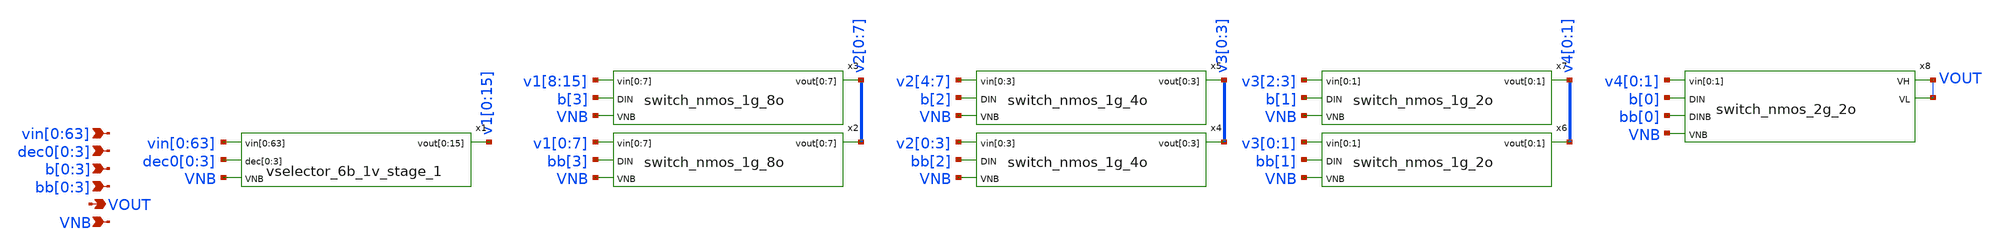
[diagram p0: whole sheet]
** sch_path: xschem/vselector_seg1.sch
**.subckt vselector_seg1
*+ vin[0],vin[1],vin[2],vin[3],vin[4],vin[5],vin[6],vin[7],vin[8],vin[9],vin[10],vin[11],vin[12],vin[13],vin[14],vin[15],vin[16],vin[17],vin[18],vin[19],vin[20],vin[21],vin[22],vin[23],vin[24],vin[25],vin[26],vin[27],vin[28],vin[29],vin[30],vin[31],vin[32],vin[33],vin[34],vin[35],vin[36],vin[37],vin[38],vin[39],vin[40],vin[41],vin[42],vin[43],vin[44],vin[45],vin[46],vin[47],vin[48],vin[49],vin[50],vin[51],vin[52],vin[53],vin[54],vin[55],vin[56],vin[57],vin[58],vin[59],vin[60],vin[61],vin[62],vin[63] VOUT VNB dec0[0],dec0[1],dec0[2],dec0[3] b[0],b[1],b[2],b[3] bb[0],bb[1],bb[2],bb[3]
*.ipin
*+ vin[0],vin[1],vin[2],vin[3],vin[4],vin[5],vin[6],vin[7],vin[8],vin[9],vin[10],vin[11],vin[12],vin[13],vin[14],vin[15],vin[16],vin[17],vin[18],vin[19],vin[20],vin[21],vin[22],vin[23],vin[24],vin[25],vin[26],vin[27],vin[28],vin[29],vin[30],vin[31],vin[32],vin[33],vin[34],vin[35],vin[36],vin[37],vin[38],vin[39],vin[40],vin[41],vin[42],vin[43],vin[44],vin[45],vin[46],vin[47],vin[48],vin[49],vin[50],vin[51],vin[52],vin[53],vin[54],vin[55],vin[56],vin[57],vin[58],vin[59],vin[60],vin[61],vin[62],vin[63]
*.opin VOUT
*.ipin VNB
*.ipin dec0[0],dec0[1],dec0[2],dec0[3]
*.ipin b[0],b[1],b[2],b[3]
*.ipin bb[0],bb[1],bb[2],bb[3]
x1 vin[0] vin[1] vin[2] vin[3] vin[4] vin[5] vin[6] vin[7] vin[8] vin[9] vin[10] vin[11] vin[12]
+ vin[13] vin[14] vin[15] vin[16] vin[17] vin[18] vin[19] vin[20] vin[21] vin[22] vin[23] vin[24] vin[25]
+ vin[26] vin[27] vin[28] vin[29] vin[30] vin[31] vin[32] vin[33] vin[34] vin[35] vin[36] vin[37] vin[38]
+ vin[39] vin[40] vin[41] vin[42] vin[43] vin[44] vin[45] vin[46] vin[47] vin[48] vin[49] vin[50] vin[51]
+ vin[52] vin[53] vin[54] vin[55] vin[56] vin[57] vin[58] vin[59] vin[60] vin[61] vin[62] vin[63] dec0[0]
+ dec0[1] dec0[2] dec0[3] v1[0] v1[1] v1[2] v1[3] v1[4] v1[5] v1[6] v1[7] v1[8] v1[9] v1[10] v1[11] v1[12]
+ v1[13] v1[14] v1[15] VNB vselector_6b_1v_stage_1
x2 v1[0] v1[1] v1[2] v1[3] v1[4] v1[5] v1[6] v1[7] bb[3] v2[0] v2[1] v2[2] v2[3] v2[4] v2[5] v2[6]
+ v2[7] VNB switch_nmos_1g_8o
x3 v1[8] v1[9] v1[10] v1[11] v1[12] v1[13] v1[14] v1[15] b[3] v2[0] v2[1] v2[2] v2[3] v2[4] v2[5]
+ v2[6] v2[7] VNB switch_nmos_1g_8o
x4 v2[0] v2[1] v2[2] v2[3] bb[2] v3[0] v3[1] v3[2] v3[3] VNB switch_nmos_1g_4o
x5 v2[4] v2[5] v2[6] v2[7] b[2] v3[0] v3[1] v3[2] v3[3] VNB switch_nmos_1g_4o
x6 v3[0] v3[1] bb[1] v4[0] v4[1] VNB switch_nmos_1g_2o
x7 v3[2] v3[3] b[1] v4[0] v4[1] VNB switch_nmos_1g_2o
x8 v4[0] v4[1] b[0] bb[0] VOUT VOUT VNB switch_nmos_2g_2o
**.ends

* expanding   symbol:  vselector_6b_1v_stage_1.sym # of pins=4
** sym_path: xschem/vselector_6b_1v_stage_1.sym
** sch_path: xschem/vselector_6b_1v_stage_1.sch
.subckt vselector_6b_1v_stage_1 vin[0] vin[1] vin[2] vin[3] vin[4] vin[5] vin[6] vin[7] vin[8]
+ vin[9] vin[10] vin[11] vin[12] vin[13] vin[14] vin[15] vin[16] vin[17] vin[18] vin[19] vin[20] vin[21]
+ vin[22] vin[23] vin[24] vin[25] vin[26] vin[27] vin[28] vin[29] vin[30] vin[31] vin[32] vin[33] vin[34]
+ vin[35] vin[36] vin[37] vin[38] vin[39] vin[40] vin[41] vin[42] vin[43] vin[44] vin[45] vin[46] vin[47]
+ vin[48] vin[49] vin[50] vin[51] vin[52] vin[53] vin[54] vin[55] vin[56] vin[57] vin[58] vin[59] vin[60]
+ vin[61] vin[62] vin[63] dec[0] dec[1] dec[2] dec[3] vout[0] vout[1] vout[2] vout[3] vout[4] vout[5] vout[6]
+ vout[7] vout[8] vout[9] vout[10] vout[11] vout[12] vout[13] vout[14] vout[15] VNB
*.ipin
*+ vin[0],vin[1],vin[2],vin[3],vin[4],vin[5],vin[6],vin[7],vin[8],vin[9],vin[10],vin[11],vin[12],vin[13],vin[14],vin[15],vin[16],vin[17],vin[18],vin[19],vin[20],vin[21],vin[22],vin[23],vin[24],vin[25],vin[26],vin[27],vin[28],vin[29],vin[30],vin[31],vin[32],vin[33],vin[34],vin[35],vin[36],vin[37],vin[38],vin[39],vin[40],vin[41],vin[42],vin[43],vin[44],vin[45],vin[46],vin[47],vin[48],vin[49],vin[50],vin[51],vin[52],vin[53],vin[54],vin[55],vin[56],vin[57],vin[58],vin[59],vin[60],vin[61],vin[62],vin[63]
*.opin
*+ vout[0],vout[1],vout[2],vout[3],vout[4],vout[5],vout[6],vout[7],vout[8],vout[9],vout[10],vout[11],vout[12],vout[13],vout[14],vout[15]
*.ipin VNB
*.ipin dec[0],dec[1],dec[2],dec[3]
x1 vin[48] vin[49] vin[50] vin[51] vin[52] vin[53] vin[54] vin[55] vin[56] vin[57] vin[58] vin[59]
+ vin[60] vin[61] vin[62] vin[63] dec[3] vout[0] vout[1] vout[2] vout[3] vout[4] vout[5] vout[6] vout[7]
+ vout[8] vout[9] vout[10] vout[11] vout[12] vout[13] vout[14] vout[15] VNB vselector_16b_1v
x2 vin[32] vin[33] vin[34] vin[35] vin[36] vin[37] vin[38] vin[39] vin[40] vin[41] vin[42] vin[43]
+ vin[44] vin[45] vin[46] vin[47] dec[2] vout[0] vout[1] vout[2] vout[3] vout[4] vout[5] vout[6] vout[7]
+ vout[8] vout[9] vout[10] vout[11] vout[12] vout[13] vout[14] vout[15] VNB vselector_16b_1v
x3 vin[16] vin[17] vin[18] vin[19] vin[20] vin[21] vin[22] vin[23] vin[24] vin[25] vin[26] vin[27]
+ vin[28] vin[29] vin[30] vin[31] dec[1] vout[0] vout[1] vout[2] vout[3] vout[4] vout[5] vout[6] vout[7]
+ vout[8] vout[9] vout[10] vout[11] vout[12] vout[13] vout[14] vout[15] VNB vselector_16b_1v
x4 vin[0] vin[1] vin[2] vin[3] vin[4] vin[5] vin[6] vin[7] vin[8] vin[9] vin[10] vin[11] vin[12]
+ vin[13] vin[14] vin[15] dec[0] vout[0] vout[1] vout[2] vout[3] vout[4] vout[5] vout[6] vout[7] vout[8]
+ vout[9] vout[10] vout[11] vout[12] vout[13] vout[14] vout[15] VNB vselector_16b_1v
.ends


* expanding   symbol:  switch_nmos_1g_8o.sym # of pins=4
** sym_path: xschem/switch_nmos_1g_8o.sym
** sch_path: xschem/switch_nmos_1g_8o.sch
.subckt switch_nmos_1g_8o vin[0] vin[1] vin[2] vin[3] vin[4] vin[5] vin[6] vin[7] DIN vout[0]
+ vout[1] vout[2] vout[3] vout[4] vout[5] vout[6] vout[7] VNB
*.ipin vin[0],vin[1],vin[2],vin[3],vin[4],vin[5],vin[6],vin[7]
*.opin vout[0],vout[1],vout[2],vout[3],vout[4],vout[5],vout[6],vout[7]
*.ipin VNB
*.ipin DIN
.param wp=0.42 wn=0.42 l=0.5

XM1 vin[0] DIN vout[0] VNB sky130_fd_pr__nfet_g5v0d10v5 L=l W=wn nf=1 ad='int((nf+1)/2) * W/nf * 0.29'
+ as='int((nf+2)/2) * W/nf * 0.29' pd='2*int((nf+1)/2) * (W/nf + 0.29)' ps='2*int((nf+2)/2) * (W/nf + 0.29)'
+ nrd='0.29 / W' nrs='0.29 / W' sa=0 sb=0 sd=0 mult=1 m=1
XM2 vin[1] DIN vout[1] VNB sky130_fd_pr__nfet_g5v0d10v5 L=l W=wn nf=1 ad='int((nf+1)/2) * W/nf * 0.29'
+ as='int((nf+2)/2) * W/nf * 0.29' pd='2*int((nf+1)/2) * (W/nf + 0.29)' ps='2*int((nf+2)/2) * (W/nf + 0.29)'
+ nrd='0.29 / W' nrs='0.29 / W' sa=0 sb=0 sd=0 mult=1 m=1
XM3 vin[2] DIN vout[2] VNB sky130_fd_pr__nfet_g5v0d10v5 L=l W=wn nf=1 ad='int((nf+1)/2) * W/nf * 0.29'
+ as='int((nf+2)/2) * W/nf * 0.29' pd='2*int((nf+1)/2) * (W/nf + 0.29)' ps='2*int((nf+2)/2) * (W/nf + 0.29)'
+ nrd='0.29 / W' nrs='0.29 / W' sa=0 sb=0 sd=0 mult=1 m=1
XM4 vin[3] DIN vout[3] VNB sky130_fd_pr__nfet_g5v0d10v5 L=l W=wn nf=1 ad='int((nf+1)/2) * W/nf * 0.29'
+ as='int((nf+2)/2) * W/nf * 0.29' pd='2*int((nf+1)/2) * (W/nf + 0.29)' ps='2*int((nf+2)/2) * (W/nf + 0.29)'
+ nrd='0.29 / W' nrs='0.29 / W' sa=0 sb=0 sd=0 mult=1 m=1
XM5 vin[4] DIN vout[4] VNB sky130_fd_pr__nfet_g5v0d10v5 L=l W=wn nf=1 ad='int((nf+1)/2) * W/nf * 0.29'
+ as='int((nf+2)/2) * W/nf * 0.29' pd='2*int((nf+1)/2) * (W/nf + 0.29)' ps='2*int((nf+2)/2) * (W/nf + 0.29)'
+ nrd='0.29 / W' nrs='0.29 / W' sa=0 sb=0 sd=0 mult=1 m=1
XM6 vin[5] DIN vout[5] VNB sky130_fd_pr__nfet_g5v0d10v5 L=l W=wn nf=1 ad='int((nf+1)/2) * W/nf * 0.29'
+ as='int((nf+2)/2) * W/nf * 0.29' pd='2*int((nf+1)/2) * (W/nf + 0.29)' ps='2*int((nf+2)/2) * (W/nf + 0.29)'
+ nrd='0.29 / W' nrs='0.29 / W' sa=0 sb=0 sd=0 mult=1 m=1
XM7 vin[6] DIN vout[6] VNB sky130_fd_pr__nfet_g5v0d10v5 L=l W=wn nf=1 ad='int((nf+1)/2) * W/nf * 0.29'
+ as='int((nf+2)/2) * W/nf * 0.29' pd='2*int((nf+1)/2) * (W/nf + 0.29)' ps='2*int((nf+2)/2) * (W/nf + 0.29)'
+ nrd='0.29 / W' nrs='0.29 / W' sa=0 sb=0 sd=0 mult=1 m=1
XM8 vin[7] DIN vout[7] VNB sky130_fd_pr__nfet_g5v0d10v5 L=l W=wn nf=1 ad='int((nf+1)/2) * W/nf * 0.29'
+ as='int((nf+2)/2) * W/nf * 0.29' pd='2*int((nf+1)/2) * (W/nf + 0.29)' ps='2*int((nf+2)/2) * (W/nf + 0.29)'
+ nrd='0.29 / W' nrs='0.29 / W' sa=0 sb=0 sd=0 mult=1 m=1
.ends


* expanding   symbol:  switch_nmos_1g_4o.sym # of pins=4
** sym_path: xschem/switch_nmos_1g_4o.sym
** sch_path: xschem/switch_nmos_1g_4o.sch
.subckt switch_nmos_1g_4o vin[0] vin[1] vin[2] vin[3] DIN vout[0] vout[1] vout[2] vout[3] VNB
*.ipin vin[0],vin[1],vin[2],vin[3]
*.opin vout[0],vout[1],vout[2],vout[3]
*.ipin VNB
*.ipin DIN
.param wp=0.42 wn=0.42 l=0.5

XM1 vin[0] DIN vout[0] VNB sky130_fd_pr__nfet_g5v0d10v5 L=l W=wn nf=1 ad='int((nf+1)/2) * W/nf * 0.29'
+ as='int((nf+2)/2) * W/nf * 0.29' pd='2*int((nf+1)/2) * (W/nf + 0.29)' ps='2*int((nf+2)/2) * (W/nf + 0.29)'
+ nrd='0.29 / W' nrs='0.29 / W' sa=0 sb=0 sd=0 mult=1 m=1
XM2 vin[1] DIN vout[1] VNB sky130_fd_pr__nfet_g5v0d10v5 L=l W=wn nf=1 ad='int((nf+1)/2) * W/nf * 0.29'
+ as='int((nf+2)/2) * W/nf * 0.29' pd='2*int((nf+1)/2) * (W/nf + 0.29)' ps='2*int((nf+2)/2) * (W/nf + 0.29)'
+ nrd='0.29 / W' nrs='0.29 / W' sa=0 sb=0 sd=0 mult=1 m=1
XM3 vin[2] DIN vout[2] VNB sky130_fd_pr__nfet_g5v0d10v5 L=l W=wn nf=1 ad='int((nf+1)/2) * W/nf * 0.29'
+ as='int((nf+2)/2) * W/nf * 0.29' pd='2*int((nf+1)/2) * (W/nf + 0.29)' ps='2*int((nf+2)/2) * (W/nf + 0.29)'
+ nrd='0.29 / W' nrs='0.29 / W' sa=0 sb=0 sd=0 mult=1 m=1
XM4 vin[3] DIN vout[3] VNB sky130_fd_pr__nfet_g5v0d10v5 L=l W=wn nf=1 ad='int((nf+1)/2) * W/nf * 0.29'
+ as='int((nf+2)/2) * W/nf * 0.29' pd='2*int((nf+1)/2) * (W/nf + 0.29)' ps='2*int((nf+2)/2) * (W/nf + 0.29)'
+ nrd='0.29 / W' nrs='0.29 / W' sa=0 sb=0 sd=0 mult=1 m=1
.ends


* expanding   symbol:  switch_nmos_1g_2o.sym # of pins=4
** sym_path: xschem/switch_nmos_1g_2o.sym
** sch_path: xschem/switch_nmos_1g_2o.sch
.subckt switch_nmos_1g_2o vin[0] vin[1] DIN vout[0] vout[1] VNB
*.ipin vin[0],vin[1]
*.opin vout[0],vout[1]
*.ipin VNB
*.ipin DIN
.param wp=0.42 wn=0.42 l=0.5

XM2 vin[1] DIN vout[1] VNB sky130_fd_pr__nfet_g5v0d10v5 L=l W=wn nf=1 ad='int((nf+1)/2) * W/nf * 0.29'
+ as='int((nf+2)/2) * W/nf * 0.29' pd='2*int((nf+1)/2) * (W/nf + 0.29)' ps='2*int((nf+2)/2) * (W/nf + 0.29)'
+ nrd='0.29 / W' nrs='0.29 / W' sa=0 sb=0 sd=0 mult=1 m=1
XM1 vin[0] DIN vout[0] VNB sky130_fd_pr__nfet_g5v0d10v5 L=l W=wn nf=1 ad='int((nf+1)/2) * W/nf * 0.29'
+ as='int((nf+2)/2) * W/nf * 0.29' pd='2*int((nf+1)/2) * (W/nf + 0.29)' ps='2*int((nf+2)/2) * (W/nf + 0.29)'
+ nrd='0.29 / W' nrs='0.29 / W' sa=0 sb=0 sd=0 mult=1 m=1
.ends


* expanding   symbol:  switch_nmos_2g_2o.sym # of pins=6
** sym_path: xschem/switch_nmos_2g_2o.sym
** sch_path: xschem/switch_nmos_2g_2o.sch
.subckt switch_nmos_2g_2o vin[0] vin[1] DIN DINB VH VL VNB
*.ipin vin[0],vin[1]
*.opin VH
*.ipin VNB
*.ipin DIN
*.opin VL
*.ipin DINB
.param wp=0.42 wn=0.42 l=0.5

XM1 vin[0] DINB VL VNB sky130_fd_pr__nfet_g5v0d10v5 L=l W=wn nf=1 ad='int((nf+1)/2) * W/nf * 0.29' as='int((nf+2)/2) * W/nf * 0.29'
+ pd='2*int((nf+1)/2) * (W/nf + 0.29)' ps='2*int((nf+2)/2) * (W/nf + 0.29)' nrd='0.29 / W' nrs='0.29 / W'
+ sa=0 sb=0 sd=0 mult=1 m=1
XM2 vin[1] DIN VH VNB sky130_fd_pr__nfet_g5v0d10v5 L=l W=wn nf=1 ad='int((nf+1)/2) * W/nf * 0.29' as='int((nf+2)/2) * W/nf * 0.29'
+ pd='2*int((nf+1)/2) * (W/nf + 0.29)' ps='2*int((nf+2)/2) * (W/nf + 0.29)' nrd='0.29 / W' nrs='0.29 / W'
+ sa=0 sb=0 sd=0 mult=1 m=1
.ends


* expanding   symbol:  vselector_16b_1v.sym # of pins=4
** sym_path: xschem/vselector_16b_1v.sym
** sch_path: xschem/vselector_16b_1v.sch
.subckt vselector_16b_1v vin[0] vin[1] vin[2] vin[3] vin[4] vin[5] vin[6] vin[7] vin[8] vin[9]
+ vin[10] vin[11] vin[12] vin[13] vin[14] vin[15] DIN vout[0] vout[1] vout[2] vout[3] vout[4] vout[5] vout[6]
+ vout[7] vout[8] vout[9] vout[10] vout[11] vout[12] vout[13] vout[14] vout[15] VNB
*.ipin
*+ vin[0],vin[1],vin[2],vin[3],vin[4],vin[5],vin[6],vin[7],vin[8],vin[9],vin[10],vin[11],vin[12],vin[13],vin[14],vin[15]
*.opin
*+ vout[0],vout[1],vout[2],vout[3],vout[4],vout[5],vout[6],vout[7],vout[8],vout[9],vout[10],vout[11],vout[12],vout[13],vout[14],vout[15]
*.ipin VNB
*.ipin DIN
.param wp=0.42 wn=0.42 l=0.5

XM1 vout[0] DIN vin[0] VNB sky130_fd_pr__nfet_g5v0d10v5 L=l W=wn nf=1 ad='int((nf+1)/2) * W/nf * 0.29'
+ as='int((nf+2)/2) * W/nf * 0.29' pd='2*int((nf+1)/2) * (W/nf + 0.29)' ps='2*int((nf+2)/2) * (W/nf + 0.29)'
+ nrd='0.29 / W' nrs='0.29 / W' sa=0 sb=0 sd=0 mult=1 m=1
XM2 vout[1] DIN vin[1] VNB sky130_fd_pr__nfet_g5v0d10v5 L=l W=wn nf=1 ad='int((nf+1)/2) * W/nf * 0.29'
+ as='int((nf+2)/2) * W/nf * 0.29' pd='2*int((nf+1)/2) * (W/nf + 0.29)' ps='2*int((nf+2)/2) * (W/nf + 0.29)'
+ nrd='0.29 / W' nrs='0.29 / W' sa=0 sb=0 sd=0 mult=1 m=1
XM3 vout[2] DIN vin[2] VNB sky130_fd_pr__nfet_g5v0d10v5 L=l W=wn nf=1 ad='int((nf+1)/2) * W/nf * 0.29'
+ as='int((nf+2)/2) * W/nf * 0.29' pd='2*int((nf+1)/2) * (W/nf + 0.29)' ps='2*int((nf+2)/2) * (W/nf + 0.29)'
+ nrd='0.29 / W' nrs='0.29 / W' sa=0 sb=0 sd=0 mult=1 m=1
XM4 vout[3] DIN vin[3] VNB sky130_fd_pr__nfet_g5v0d10v5 L=l W=wn nf=1 ad='int((nf+1)/2) * W/nf * 0.29'
+ as='int((nf+2)/2) * W/nf * 0.29' pd='2*int((nf+1)/2) * (W/nf + 0.29)' ps='2*int((nf+2)/2) * (W/nf + 0.29)'
+ nrd='0.29 / W' nrs='0.29 / W' sa=0 sb=0 sd=0 mult=1 m=1
XM5 vout[4] DIN vin[4] VNB sky130_fd_pr__nfet_g5v0d10v5 L=l W=wn nf=1 ad='int((nf+1)/2) * W/nf * 0.29'
+ as='int((nf+2)/2) * W/nf * 0.29' pd='2*int((nf+1)/2) * (W/nf + 0.29)' ps='2*int((nf+2)/2) * (W/nf + 0.29)'
+ nrd='0.29 / W' nrs='0.29 / W' sa=0 sb=0 sd=0 mult=1 m=1
XM6 vout[5] DIN vin[5] VNB sky130_fd_pr__nfet_g5v0d10v5 L=l W=wn nf=1 ad='int((nf+1)/2) * W/nf * 0.29'
+ as='int((nf+2)/2) * W/nf * 0.29' pd='2*int((nf+1)/2) * (W/nf + 0.29)' ps='2*int((nf+2)/2) * (W/nf + 0.29)'
+ nrd='0.29 / W' nrs='0.29 / W' sa=0 sb=0 sd=0 mult=1 m=1
XM7 vout[6] DIN vin[6] VNB sky130_fd_pr__nfet_g5v0d10v5 L=l W=wn nf=1 ad='int((nf+1)/2) * W/nf * 0.29'
+ as='int((nf+2)/2) * W/nf * 0.29' pd='2*int((nf+1)/2) * (W/nf + 0.29)' ps='2*int((nf+2)/2) * (W/nf + 0.29)'
+ nrd='0.29 / W' nrs='0.29 / W' sa=0 sb=0 sd=0 mult=1 m=1
XM8 vout[7] DIN vin[7] VNB sky130_fd_pr__nfet_g5v0d10v5 L=l W=wn nf=1 ad='int((nf+1)/2) * W/nf * 0.29'
+ as='int((nf+2)/2) * W/nf * 0.29' pd='2*int((nf+1)/2) * (W/nf + 0.29)' ps='2*int((nf+2)/2) * (W/nf + 0.29)'
+ nrd='0.29 / W' nrs='0.29 / W' sa=0 sb=0 sd=0 mult=1 m=1
XM9 vout[8] DIN vin[8] VNB sky130_fd_pr__nfet_g5v0d10v5 L=l W=wn nf=1 ad='int((nf+1)/2) * W/nf * 0.29'
+ as='int((nf+2)/2) * W/nf * 0.29' pd='2*int((nf+1)/2) * (W/nf + 0.29)' ps='2*int((nf+2)/2) * (W/nf + 0.29)'
+ nrd='0.29 / W' nrs='0.29 / W' sa=0 sb=0 sd=0 mult=1 m=1
XM10 vout[9] DIN vin[9] VNB sky130_fd_pr__nfet_g5v0d10v5 L=l W=wn nf=1 ad='int((nf+1)/2) * W/nf * 0.29'
+ as='int((nf+2)/2) * W/nf * 0.29' pd='2*int((nf+1)/2) * (W/nf + 0.29)' ps='2*int((nf+2)/2) * (W/nf + 0.29)'
+ nrd='0.29 / W' nrs='0.29 / W' sa=0 sb=0 sd=0 mult=1 m=1
XM11 vout[10] DIN vin[10] VNB sky130_fd_pr__nfet_g5v0d10v5 L=l W=wn nf=1 ad='int((nf+1)/2) * W/nf * 0.29'
+ as='int((nf+2)/2) * W/nf * 0.29' pd='2*int((nf+1)/2) * (W/nf + 0.29)' ps='2*int((nf+2)/2) * (W/nf + 0.29)'
+ nrd='0.29 / W' nrs='0.29 / W' sa=0 sb=0 sd=0 mult=1 m=1
XM12 vout[11] DIN vin[11] VNB sky130_fd_pr__nfet_g5v0d10v5 L=l W=wn nf=1 ad='int((nf+1)/2) * W/nf * 0.29'
+ as='int((nf+2)/2) * W/nf * 0.29' pd='2*int((nf+1)/2) * (W/nf + 0.29)' ps='2*int((nf+2)/2) * (W/nf + 0.29)'
+ nrd='0.29 / W' nrs='0.29 / W' sa=0 sb=0 sd=0 mult=1 m=1
XM13 vout[12] DIN vin[12] VNB sky130_fd_pr__nfet_g5v0d10v5 L=l W=wn nf=1 ad='int((nf+1)/2) * W/nf * 0.29'
+ as='int((nf+2)/2) * W/nf * 0.29' pd='2*int((nf+1)/2) * (W/nf + 0.29)' ps='2*int((nf+2)/2) * (W/nf + 0.29)'
+ nrd='0.29 / W' nrs='0.29 / W' sa=0 sb=0 sd=0 mult=1 m=1
XM14 vout[13] DIN vin[13] VNB sky130_fd_pr__nfet_g5v0d10v5 L=l W=wn nf=1 ad='int((nf+1)/2) * W/nf * 0.29'
+ as='int((nf+2)/2) * W/nf * 0.29' pd='2*int((nf+1)/2) * (W/nf + 0.29)' ps='2*int((nf+2)/2) * (W/nf + 0.29)'
+ nrd='0.29 / W' nrs='0.29 / W' sa=0 sb=0 sd=0 mult=1 m=1
XM15 vout[14] DIN vin[14] VNB sky130_fd_pr__nfet_g5v0d10v5 L=l W=wn nf=1 ad='int((nf+1)/2) * W/nf * 0.29'
+ as='int((nf+2)/2) * W/nf * 0.29' pd='2*int((nf+1)/2) * (W/nf + 0.29)' ps='2*int((nf+2)/2) * (W/nf + 0.29)'
+ nrd='0.29 / W' nrs='0.29 / W' sa=0 sb=0 sd=0 mult=1 m=1
XM16 vout[15] DIN vin[15] VNB sky130_fd_pr__nfet_g5v0d10v5 L=l W=wn nf=1 ad='int((nf+1)/2) * W/nf * 0.29'
+ as='int((nf+2)/2) * W/nf * 0.29' pd='2*int((nf+1)/2) * (W/nf + 0.29)' ps='2*int((nf+2)/2) * (W/nf + 0.29)'
+ nrd='0.29 / W' nrs='0.29 / W' sa=0 sb=0 sd=0 mult=1 m=1
.ends

.end
